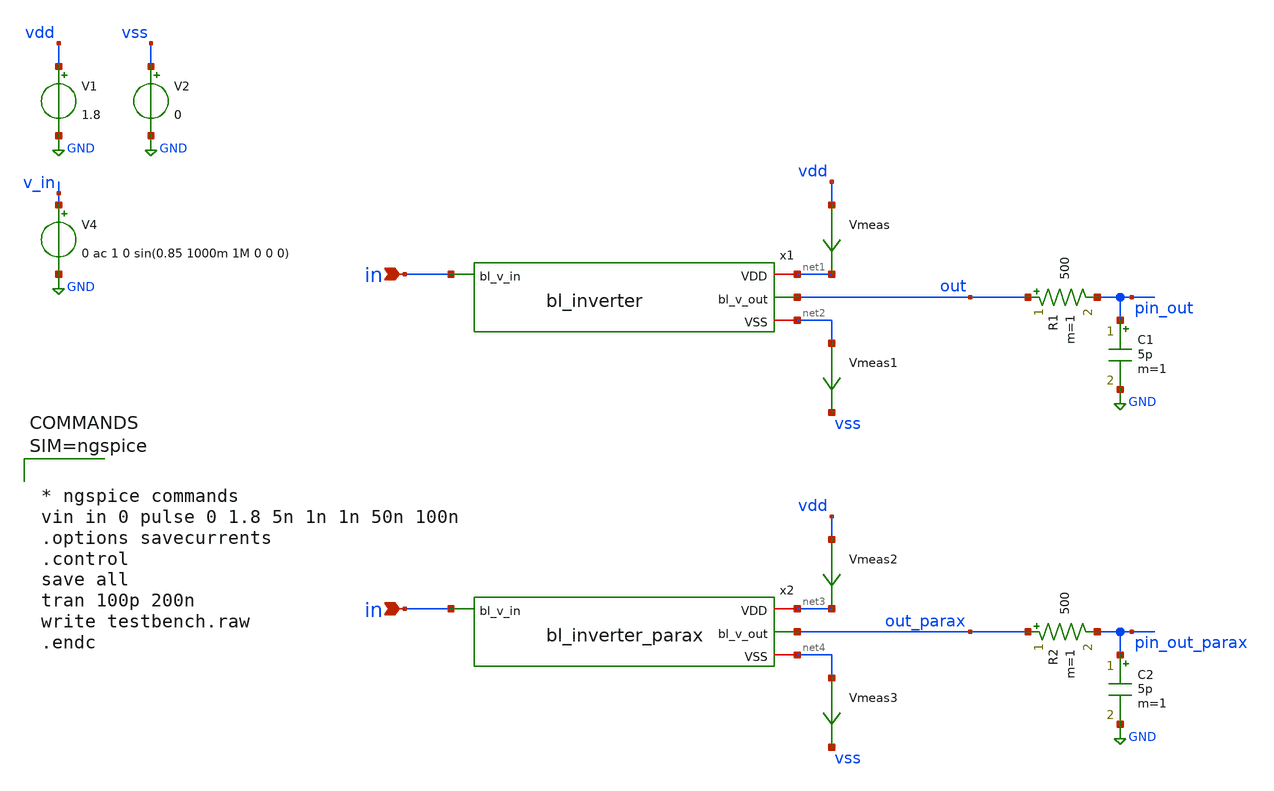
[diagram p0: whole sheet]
** sch_path: xschem/testbench.sch
**.subckt testbench in in
*.ipin in
*.ipin in
x1 net1 in out net2 bl_inverter
V1 vdd GND 1.8
V2 vss GND 0
R1 out pin_out 500 m=1
C1 pin_out GND 5p m=1
V4 v_in GND 0 ac 1 0 sin(0.85 1000m 1M 0 0 0)
Vmeas vdd net1 0
.save i(vmeas)
Vmeas1 net2 vss 0
.save i(vmeas1)
x2 net3 in out_parax net4 bl_inverter_parax
R2 out_parax pin_out_parax 500 m=1
C2 pin_out_parax GND 5p m=1
Vmeas2 vdd net3 0
.save i(vmeas2)
Vmeas3 net4 vss 0
.save i(vmeas3)
**** begin user architecture code

** opencircuitdesign pdks install
.lib $::SKYWATER_MODELS/sky130.lib.spice tt





* ngspice commands
vin in 0 pulse 0 1.8 5n 1n 1n 50n 100n
.options savecurrents
.control
save all
tran 100p 200n
write testbench.raw
.endc



**** end user architecture code
**.ends

* expanding   symbol:  bl_inverter.sym # of pins=4
** sym_path: xschem/bl_inverter.sym
** sch_path: xschem/bl_inverter.sch
.subckt bl_inverter VDD bl_v_in bl_v_out VSS
*.iopin VDD
*.iopin VSS
*.ipin bl_v_in
*.opin bl_v_out
XM2 bl_v_1 bl_v_in VSS VSS sky130_fd_pr__nfet_01v8 L=0.15 W=1 nf=1 ad='int((nf+1)/2) * W/nf * 0.29' as='int((nf+2)/2) * W/nf * 0.29'
+ pd='2*int((nf+1)/2) * (W/nf + 0.29)' ps='2*int((nf+2)/2) * (W/nf + 0.29)' nrd='0.29 / W' nrs='0.29 / W'
+ sa=0 sb=0 sd=0 mult=1 m=1
XM4 bl_v_out bl_v_1 VSS VSS sky130_fd_pr__nfet_01v8 L=0.15 W=20 nf=20 ad='int((nf+1)/2) * W/nf * 0.29'
+ as='int((nf+2)/2) * W/nf * 0.29' pd='2*int((nf+1)/2) * (W/nf + 0.29)' ps='2*int((nf+2)/2) * (W/nf + 0.29)'
+ nrd='0.29 / W' nrs='0.29 / W' sa=0 sb=0 sd=0 mult=1 m=1
XM5 bl_v_1 bl_v_in VDD VDD sky130_fd_pr__pfet_01v8 L=0.15 W=1 nf=1 ad='int((nf+1)/2) * W/nf * 0.29' as='int((nf+2)/2) * W/nf * 0.29'
+ pd='2*int((nf+1)/2) * (W/nf + 0.29)' ps='2*int((nf+2)/2) * (W/nf + 0.29)' nrd='0.29 / W' nrs='0.29 / W'
+ sa=0 sb=0 sd=0 mult=1 m=1
XM1 bl_v_out bl_v_1 VDD VDD sky130_fd_pr__pfet_01v8 L=0.15 W=20 nf=20 ad='int((nf+1)/2) * W/nf * 0.29'
+ as='int((nf+2)/2) * W/nf * 0.29' pd='2*int((nf+1)/2) * (W/nf + 0.29)' ps='2*int((nf+2)/2) * (W/nf + 0.29)'
+ nrd='0.29 / W' nrs='0.29 / W' sa=0 sb=0 sd=0 mult=1 m=1
.ends


* expanding   symbol:  bl_inverter_parax.sym # of pins=4
** sym_path: xschem/bl_inverter.sym
.include [file normalize ../mag/bl_inverter.sim.spice]
.GLOBAL GND
.end
